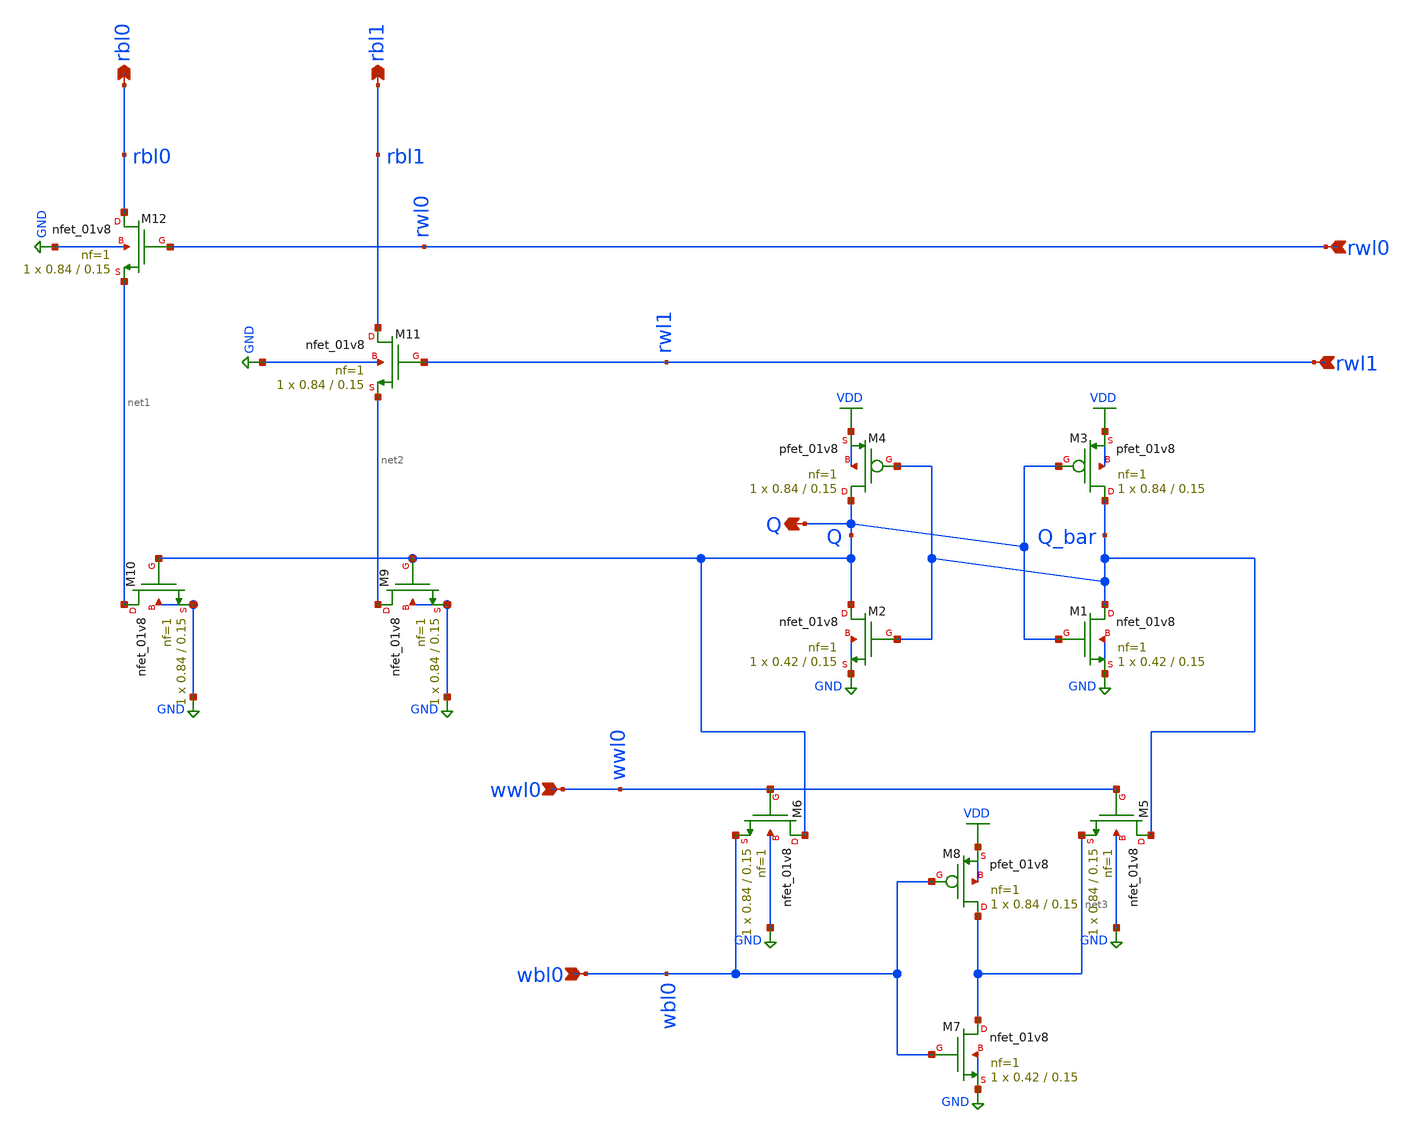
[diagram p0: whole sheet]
** sch_path: xschem/cell_2r1w.sch
**.subckt cell_2r1w rwl1 rwl0 wwl0 wbl0 rbl1 rbl0 Q
*.ipin rwl1
*.ipin rwl0
*.ipin wwl0
*.ipin wbl0
*.opin rbl1
*.opin rbl0
*.opin Q
XM1 Q_bar Q GND GND sky130_fd_pr__nfet_01v8 L=0.15 W=0.42 nf=1 ad='int((nf+1)/2) * W/nf * 0.29' as='int((nf+2)/2) * W/nf * 0.29'
+ pd='2*int((nf+1)/2) * (W/nf + 0.29)' ps='2*int((nf+2)/2) * (W/nf + 0.29)' nrd='0.29 / W' nrs='0.29 / W'
+ sa=0 sb=0 sd=0 mult=1 m=1
XM2 Q Q_bar GND GND sky130_fd_pr__nfet_01v8 L=0.15 W=0.42 nf=1 ad='int((nf+1)/2) * W/nf * 0.29' as='int((nf+2)/2) * W/nf * 0.29'
+ pd='2*int((nf+1)/2) * (W/nf + 0.29)' ps='2*int((nf+2)/2) * (W/nf + 0.29)' nrd='0.29 / W' nrs='0.29 / W'
+ sa=0 sb=0 sd=0 mult=1 m=1
XM3 Q_bar Q VDD VDD sky130_fd_pr__pfet_01v8 L=0.15 W=0.84 nf=1 ad='int((nf+1)/2) * W/nf * 0.29' as='int((nf+2)/2) * W/nf * 0.29'
+ pd='2*int((nf+1)/2) * (W/nf + 0.29)' ps='2*int((nf+2)/2) * (W/nf + 0.29)' nrd='0.29 / W' nrs='0.29 / W'
+ sa=0 sb=0 sd=0 mult=1 m=1
XM4 Q Q_bar VDD VDD sky130_fd_pr__pfet_01v8 L=0.15 W=0.84 nf=1 ad='int((nf+1)/2) * W/nf * 0.29' as='int((nf+2)/2) * W/nf * 0.29'
+ pd='2*int((nf+1)/2) * (W/nf + 0.29)' ps='2*int((nf+2)/2) * (W/nf + 0.29)' nrd='0.29 / W' nrs='0.29 / W'
+ sa=0 sb=0 sd=0 mult=1 m=1
XM5 Q_bar wwl0 net3 GND sky130_fd_pr__nfet_01v8 L=0.15 W=0.84 nf=1 ad='int((nf+1)/2) * W/nf * 0.29' as='int((nf+2)/2) * W/nf * 0.29'
+ pd='2*int((nf+1)/2) * (W/nf + 0.29)' ps='2*int((nf+2)/2) * (W/nf + 0.29)' nrd='0.29 / W' nrs='0.29 / W'
+ sa=0 sb=0 sd=0 mult=1 m=1
XM6 Q wwl0 wbl0 GND sky130_fd_pr__nfet_01v8 L=0.15 W=0.84 nf=1 ad='int((nf+1)/2) * W/nf * 0.29' as='int((nf+2)/2) * W/nf * 0.29'
+ pd='2*int((nf+1)/2) * (W/nf + 0.29)' ps='2*int((nf+2)/2) * (W/nf + 0.29)' nrd='0.29 / W' nrs='0.29 / W'
+ sa=0 sb=0 sd=0 mult=1 m=1
XM7 net3 wbl0 GND GND sky130_fd_pr__nfet_01v8 L=0.15 W=0.42 nf=1 ad='int((nf+1)/2) * W/nf * 0.29' as='int((nf+2)/2) * W/nf * 0.29'
+ pd='2*int((nf+1)/2) * (W/nf + 0.29)' ps='2*int((nf+2)/2) * (W/nf + 0.29)' nrd='0.29 / W' nrs='0.29 / W'
+ sa=0 sb=0 sd=0 mult=1 m=1
XM8 net3 wbl0 VDD VDD sky130_fd_pr__pfet_01v8 L=0.15 W=0.84 nf=1 ad='int((nf+1)/2) * W/nf * 0.29' as='int((nf+2)/2) * W/nf * 0.29'
+ pd='2*int((nf+1)/2) * (W/nf + 0.29)' ps='2*int((nf+2)/2) * (W/nf + 0.29)' nrd='0.29 / W' nrs='0.29 / W'
+ sa=0 sb=0 sd=0 mult=1 m=1
XM9 net2 Q GND GND sky130_fd_pr__nfet_01v8 L=0.15 W=0.84 nf=1 ad='int((nf+1)/2) * W/nf * 0.29' as='int((nf+2)/2) * W/nf * 0.29'
+ pd='2*int((nf+1)/2) * (W/nf + 0.29)' ps='2*int((nf+2)/2) * (W/nf + 0.29)' nrd='0.29 / W' nrs='0.29 / W'
+ sa=0 sb=0 sd=0 mult=1 m=1
XM10 net1 Q GND GND sky130_fd_pr__nfet_01v8 L=0.15 W=0.84 nf=1 ad='int((nf+1)/2) * W/nf * 0.29' as='int((nf+2)/2) * W/nf * 0.29'
+ pd='2*int((nf+1)/2) * (W/nf + 0.29)' ps='2*int((nf+2)/2) * (W/nf + 0.29)' nrd='0.29 / W' nrs='0.29 / W'
+ sa=0 sb=0 sd=0 mult=1 m=1
XM11 rbl1 rwl1 net2 GND sky130_fd_pr__nfet_01v8 L=0.15 W=0.84 nf=1 ad='int((nf+1)/2) * W/nf * 0.29' as='int((nf+2)/2) * W/nf * 0.29'
+ pd='2*int((nf+1)/2) * (W/nf + 0.29)' ps='2*int((nf+2)/2) * (W/nf + 0.29)' nrd='0.29 / W' nrs='0.29 / W'
+ sa=0 sb=0 sd=0 mult=1 m=1
XM12 rbl0 rwl0 net1 GND sky130_fd_pr__nfet_01v8 L=0.15 W=0.84 nf=1 ad='int((nf+1)/2) * W/nf * 0.29' as='int((nf+2)/2) * W/nf * 0.29'
+ pd='2*int((nf+1)/2) * (W/nf + 0.29)' ps='2*int((nf+2)/2) * (W/nf + 0.29)' nrd='0.29 / W' nrs='0.29 / W'
+ sa=0 sb=0 sd=0 mult=1 m=1
**.ends
.GLOBAL GND
.GLOBAL VDD
.end
